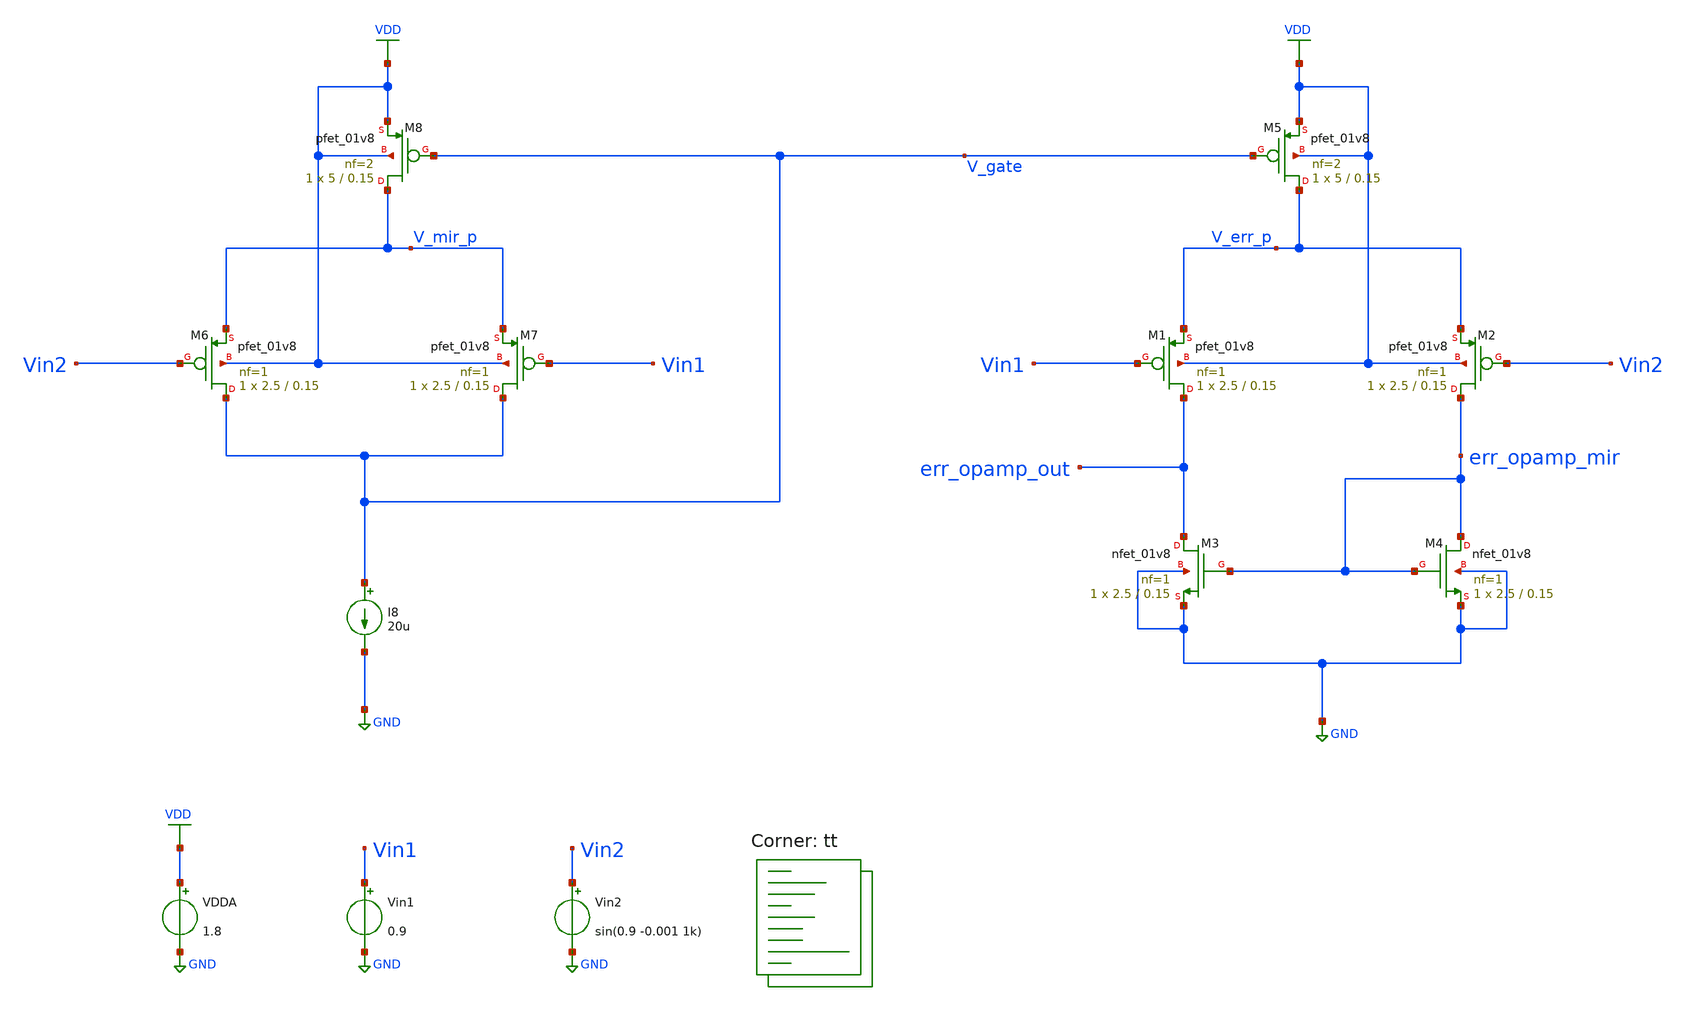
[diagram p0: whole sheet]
** sch_path: projects/opamp/xschem_ngspice/tb_err_opamp.sch
**.subckt tb_err_opamp
VDDA VDD GND 1.8
Vin1 Vin1 GND 0.9
Vin2 Vin2 GND sin(0.9 -0.001 1k)
XM2 err_opamp_mir Vin2 V_err_p VDD sky130_fd_pr__pfet_01v8 L=0.15 W=2.5 nf=1 ad='int((nf+1)/2) * W/nf * 0.29'
+ as='int((nf+2)/2) * W/nf * 0.29' pd='2*int((nf+1)/2) * (W/nf + 0.29)' ps='2*int((nf+2)/2) * (W/nf + 0.29)'
+ nrd='0.29 / W' nrs='0.29 / W' sa=0 sb=0 sd=0 mult=1 m=1
XM1 err_opamp_out Vin1 V_err_p VDD sky130_fd_pr__pfet_01v8 L=0.15 W=2.5 nf=1 ad='int((nf+1)/2) * W/nf * 0.29'
+ as='int((nf+2)/2) * W/nf * 0.29' pd='2*int((nf+1)/2) * (W/nf + 0.29)' ps='2*int((nf+2)/2) * (W/nf + 0.29)'
+ nrd='0.29 / W' nrs='0.29 / W' sa=0 sb=0 sd=0 mult=1 m=1
I8 V_gate GND 20u
XM4 err_opamp_mir err_opamp_mir GND GND sky130_fd_pr__nfet_01v8 L=0.15 W=2.5 nf=1 ad='int((nf+1)/2) * W/nf * 0.29'
+ as='int((nf+2)/2) * W/nf * 0.29' pd='2*int((nf+1)/2) * (W/nf + 0.29)' ps='2*int((nf+2)/2) * (W/nf + 0.29)'
+ nrd='0.29 / W' nrs='0.29 / W' sa=0 sb=0 sd=0 mult=1 m=1
XM3 err_opamp_out err_opamp_mir GND GND sky130_fd_pr__nfet_01v8 L=0.15 W=2.5 nf=1 ad='int((nf+1)/2) * W/nf * 0.29'
+ as='int((nf+2)/2) * W/nf * 0.29' pd='2*int((nf+1)/2) * (W/nf + 0.29)' ps='2*int((nf+2)/2) * (W/nf + 0.29)'
+ nrd='0.29 / W' nrs='0.29 / W' sa=0 sb=0 sd=0 mult=1 m=1
XM5 V_err_p V_gate VDD VDD sky130_fd_pr__pfet_01v8 L=0.15 W=5 nf=2 ad='int((nf+1)/2) * W/nf * 0.29' as='int((nf+2)/2) * W/nf * 0.29'
+ pd='2*int((nf+1)/2) * (W/nf + 0.29)' ps='2*int((nf+2)/2) * (W/nf + 0.29)' nrd='0.29 / W' nrs='0.29 / W'
+ sa=0 sb=0 sd=0 mult=1 m=1
XM6 V_gate Vin2 V_mir_p VDD sky130_fd_pr__pfet_01v8 L=0.15 W=2.5 nf=1 ad='int((nf+1)/2) * W/nf * 0.29'
+ as='int((nf+2)/2) * W/nf * 0.29' pd='2*int((nf+1)/2) * (W/nf + 0.29)' ps='2*int((nf+2)/2) * (W/nf + 0.29)'
+ nrd='0.29 / W' nrs='0.29 / W' sa=0 sb=0 sd=0 mult=1 m=1
XM7 V_gate Vin1 V_mir_p VDD sky130_fd_pr__pfet_01v8 L=0.15 W=2.5 nf=1 ad='int((nf+1)/2) * W/nf * 0.29'
+ as='int((nf+2)/2) * W/nf * 0.29' pd='2*int((nf+1)/2) * (W/nf + 0.29)' ps='2*int((nf+2)/2) * (W/nf + 0.29)'
+ nrd='0.29 / W' nrs='0.29 / W' sa=0 sb=0 sd=0 mult=1 m=1
XM8 V_mir_p V_gate VDD VDD sky130_fd_pr__pfet_01v8 L=0.15 W=5 nf=2 ad='int((nf+1)/2) * W/nf * 0.29' as='int((nf+2)/2) * W/nf * 0.29'
+ pd='2*int((nf+1)/2) * (W/nf + 0.29)' ps='2*int((nf+2)/2) * (W/nf + 0.29)' nrd='0.29 / W' nrs='0.29 / W'
+ sa=0 sb=0 sd=0 mult=1 m=1
**** begin user architecture code
.lib $::SKYWATER_MODELS/sky130.lib.spice tt




.option wnflag=1
.option savecurrents

* .param VDDGAUSS = agauss(1.8, 0.05, 1)
* .param VDD = VDDGAUSS
* .param VDD = 1.8

* .param TEMPGAUSS = agauss(40, 30, 1)
* .param temp = TEMPGAUSS
* .option temp = 26

.save @m.xm1.msky130_fd_pr__pfet_01v8[gm] @m.xm1.msky130_fd_pr__pfet_01v8[vds] @m.xm1.msky130_fd_pr__pfet_01v8[vth] @m.xm2.msky130_fd_pr__pfet_01v8[gm] @m.xm2.msky130_fd_pr__pfet_01v8[vds] @m.xm2.msky130_fd_pr__pfet_01v8[vth] @m.xm3.msky130_fd_pr__nfet_01v8[gm] @m.xm3.msky130_fd_pr__nfet_01v8[vds] @m.xm3.msky130_fd_pr__nfet_01v8[vth] @m.xm4.msky130_fd_pr__nfet_01v8[gm] @m.xm4.msky130_fd_pr__nfet_01v8[vds] @m.xm4.msky130_fd_pr__nfet_01v8[vth] @m.xm5.msky130_fd_pr__pfet_01v8[gm] @m.xm5.msky130_fd_pr__pfet_01v8[vds] @m.xm5.msky130_fd_pr__pfet_01v8[vth] @m.xm6.msky130_fd_pr__pfet_01v8[gm] @m.xm6.msky130_fd_pr__pfet_01v8[vds] @m.xm6.msky130_fd_pr__pfet_01v8[vth] @m.xm7.msky130_fd_pr__pfet_01v8[gm] @m.xm7.msky130_fd_pr__pfet_01v8[vds] @m.xm7.msky130_fd_pr__pfet_01v8[vth] @m.xm8.msky130_fd_pr__pfet_01v8[gm] @m.xm8.msky130_fd_pr__pfet_01v8[vds] @m.xm8.msky130_fd_pr__pfet_01v8[vth]

.control

  save all
  tran 1u 20m
  * ac dec 20 1 1T
  let rout=deriv(@m.xm2.msky130_fd_pr__pfet_01v8[vds])/deriv(@m.xm2.msky130_fd_pr__pfet_01v8[id])
  write tb_err_opamp.raw
  set appendwrite
  show
  * let a = deriv(@m.xm2.msky130_fd_pr__pfet_01v8[vds])
  * let b = deriv(@m.xm2.msky130_fd_pr__pfet_01v8[id])
  * plot deriv(@m.xm2.msky130_fd_pr__pfet_01v8[vds])/deriv(@m.xm2.msky130_fd_pr__pfet_01v8[id])
  * plot rout
  * plot a
.endc




**** end user architecture code
**.ends
.GLOBAL GND
.GLOBAL VDD
.end
